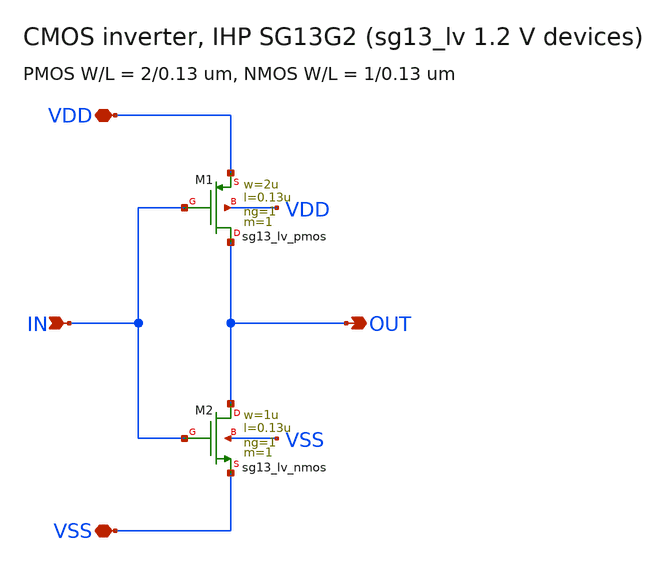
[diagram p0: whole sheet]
** sch_path: templates/ams_corners_ihp/xschem/inverter.sch
**.subckt inverter IN OUT VDD VSS
*.ipin IN
*.opin OUT
*.iopin VDD
*.iopin VSS
XM1 OUT IN VDD VDD sg13_lv_pmos w=2u l=0.13u ng=1 m=1 mm_ok=1
XM2 OUT IN VSS VSS sg13_lv_nmos w=1u l=0.13u ng=1 m=1 mm_ok=1
**.ends
.end
